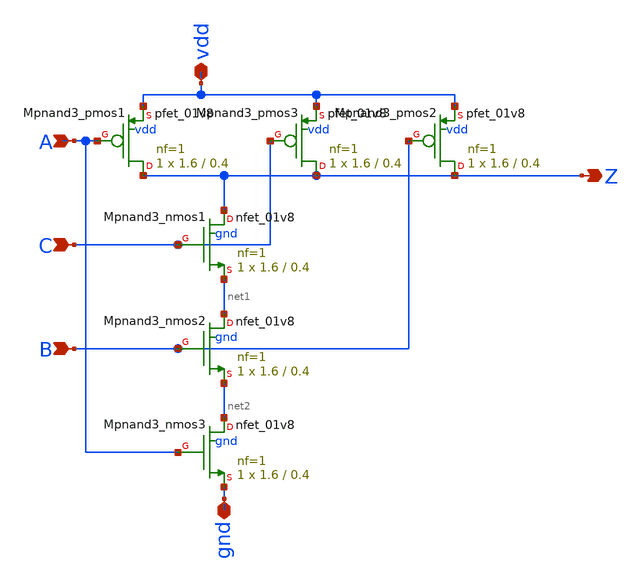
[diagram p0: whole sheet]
** sch_path: sram_2_16_scn4m/pnand3_0.sch
**.subckt pnand3_0 C A B Z vdd gnd
*.ipin C
*.ipin A
*.ipin B
*.opin Z
*.iopin vdd
*.iopin gnd
XMpnand3_nmos1 Z C net1 gnd sky130_fd_pr__nfet_01v8 L=0.4 W=1.6 nf=1 ad='int((nf+1)/2) * W/nf * 0.29'
+ as='int((nf+2)/2) * W/nf * 0.29' pd='2*int((nf+1)/2) * (W/nf + 0.29)' ps='2*int((nf+2)/2) * (W/nf + 0.29)'
+ nrd='0.29 / W' nrs='0.29 / W' sa=0 sb=0 sd=0 mult=1 m=1
XMpnand3_pmos1 Z A vdd vdd sky130_fd_pr__pfet_01v8 L=0.4 W=1.6 nf=1 ad='int((nf+1)/2) * W/nf * 0.29'
+ as='int((nf+2)/2) * W/nf * 0.29' pd='2*int((nf+1)/2) * (W/nf + 0.29)' ps='2*int((nf+2)/2) * (W/nf + 0.29)'
+ nrd='0.29 / W' nrs='0.29 / W' sa=0 sb=0 sd=0 mult=1 m=1
XMpnand3_pmos3 Z C vdd vdd sky130_fd_pr__pfet_01v8 L=0.4 W=1.6 nf=1 ad='int((nf+1)/2) * W/nf * 0.29'
+ as='int((nf+2)/2) * W/nf * 0.29' pd='2*int((nf+1)/2) * (W/nf + 0.29)' ps='2*int((nf+2)/2) * (W/nf + 0.29)'
+ nrd='0.29 / W' nrs='0.29 / W' sa=0 sb=0 sd=0 mult=1 m=1
XMpnand3_nmos2 net1 B net2 gnd sky130_fd_pr__nfet_01v8 L=0.4 W=1.6 nf=1 ad='int((nf+1)/2) * W/nf * 0.29'
+ as='int((nf+2)/2) * W/nf * 0.29' pd='2*int((nf+1)/2) * (W/nf + 0.29)' ps='2*int((nf+2)/2) * (W/nf + 0.29)'
+ nrd='0.29 / W' nrs='0.29 / W' sa=0 sb=0 sd=0 mult=1 m=1
XMpnand3_pmos2 Z B vdd vdd sky130_fd_pr__pfet_01v8 L=0.4 W=1.6 nf=1 ad='int((nf+1)/2) * W/nf * 0.29'
+ as='int((nf+2)/2) * W/nf * 0.29' pd='2*int((nf+1)/2) * (W/nf + 0.29)' ps='2*int((nf+2)/2) * (W/nf + 0.29)'
+ nrd='0.29 / W' nrs='0.29 / W' sa=0 sb=0 sd=0 mult=1 m=1
XMpnand3_nmos3 net2 A gnd gnd sky130_fd_pr__nfet_01v8 L=0.4 W=1.6 nf=1 ad='int((nf+1)/2) * W/nf * 0.29'
+ as='int((nf+2)/2) * W/nf * 0.29' pd='2*int((nf+1)/2) * (W/nf + 0.29)' ps='2*int((nf+2)/2) * (W/nf + 0.29)'
+ nrd='0.29 / W' nrs='0.29 / W' sa=0 sb=0 sd=0 mult=1 m=1
**.ends
.end
